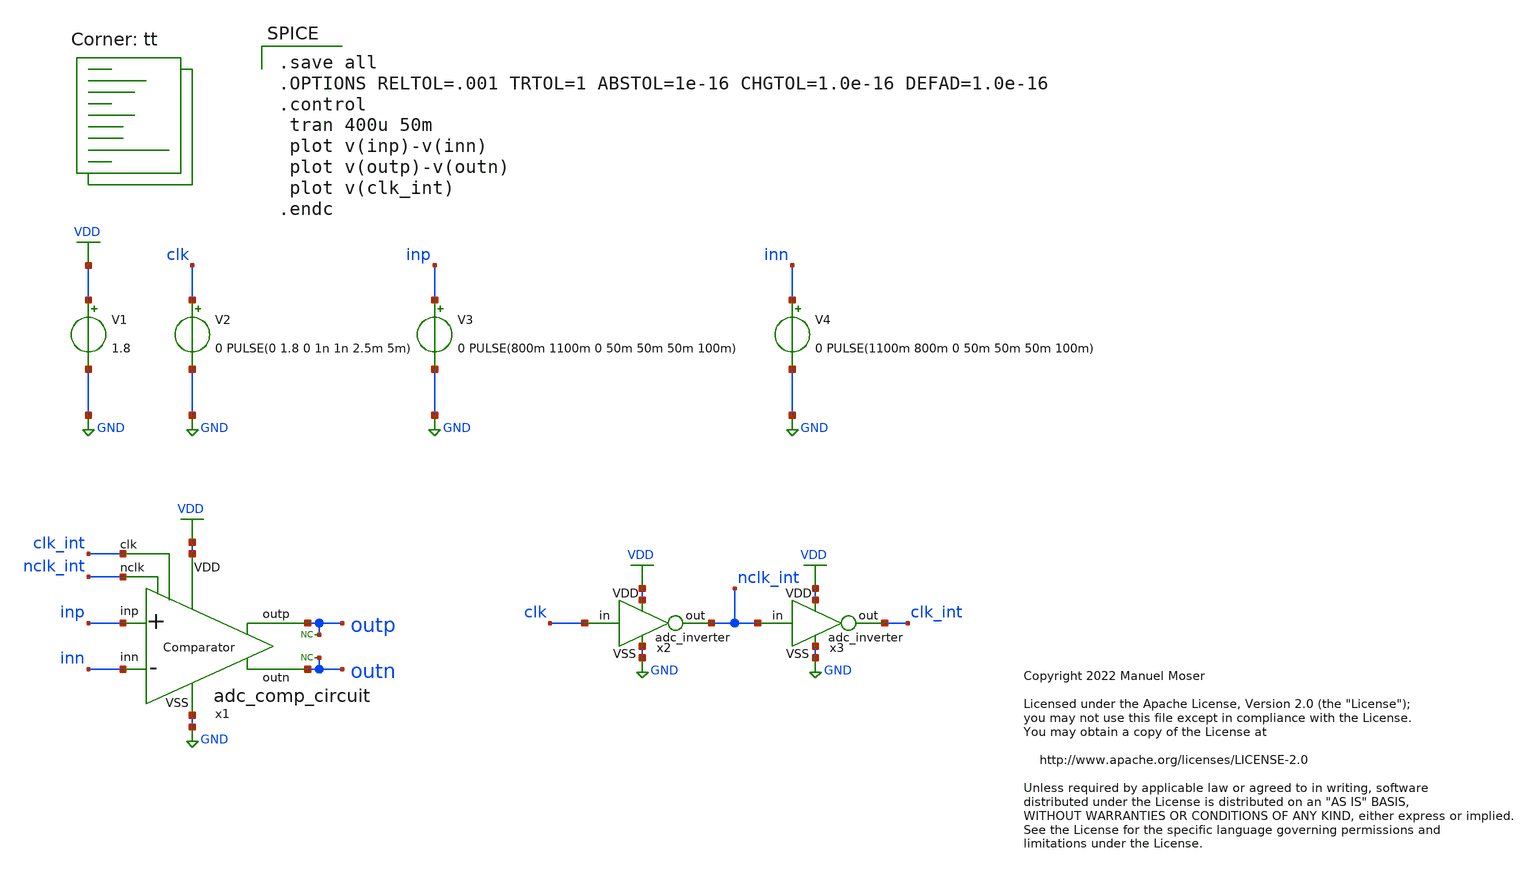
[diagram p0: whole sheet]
** sch_path: xschem/adc_comp_circuit_tb.sch
* Copyright 2022 Manuel Moser
* Licensed under the Apache License, Version 2.0 (the "License");
**.subckt adc_comp_circuit_tb
V1 VDD GND 1.8
V2 clk GND 0 PULSE(0 1.8 0 1n 1n 2.5m 5m)
V3 inp GND 0 PULSE(800m 1100m 0 50m 50m 50m 100m)
V4 inn GND 0 PULSE(1100m 800m 0 50m 50m 50m 100m)
* noconn outp
* noconn outn
x1 VDD clk_int outp inp inn outn nclk_int GND adc_comp_circuit
x2 VDD GND clk nclk_int adc_inverter
x3 VDD GND nclk_int clk_int adc_inverter
**** begin user architecture code
.lib $::SKYWATER_MODELS/sky130.lib.spice tt

.save all
.OPTIONS RELTOL=.001 TRTOL=1 ABSTOL=1e-16 CHGTOL=1.0e-16 DEFAD=1.0e-16
.control
 tran 400u 50m
 plot v(inp)-v(inn)
 plot v(outp)-v(outn)
 plot v(clk_int)
.endc

**** end user architecture code
**.ends

* expanding   symbol:  adc_comp_circuit.sym # of pins=8
** sym_path: xschem/adc_comp_circuit.sym
** sch_path: xschem/adc_comp_circuit.sch
.subckt adc_comp_circuit VDD clk outp inp inn outn nclk VSS
*.iopin VDD
*.iopin VSS
*.ipin inp
*.ipin inn
*.ipin clk
*.ipin nclk
*.opin outp
*.opin outn
XM1 on clk VDD VDD sky130_fd_pr__pfet_01v8 L=0.15 W=2 nf=4 ad='int((nf+1)/2) * W/nf * 0.29' as='int((nf+2)/2) * W/nf * 0.29'
+ pd='2*int((nf+1)/2) * (W/nf + 0.29)' ps='2*int((nf+2)/2) * (W/nf + 0.29)' nrd='0.29 / W' nrs='0.29 / W'
+ sa=0 sb=0 sd=0 mult=1 m=1
XM2 op clk VDD VDD sky130_fd_pr__pfet_01v8 L=0.15 W=2 nf=4 ad='int((nf+1)/2) * W/nf * 0.29' as='int((nf+2)/2) * W/nf * 0.29'
+ pd='2*int((nf+1)/2) * (W/nf + 0.29)' ps='2*int((nf+2)/2) * (W/nf + 0.29)' nrd='0.29 / W' nrs='0.29 / W'
+ sa=0 sb=0 sd=0 mult=1 m=1
XM3 on inp net1 VSS sky130_fd_pr__nfet_01v8 L=0.15 W=8 nf=4 ad='int((nf+1)/2) * W/nf * 0.29' as='int((nf+2)/2) * W/nf * 0.29'
+ pd='2*int((nf+1)/2) * (W/nf + 0.29)' ps='2*int((nf+2)/2) * (W/nf + 0.29)' nrd='0.29 / W' nrs='0.29 / W'
+ sa=0 sb=0 sd=0 mult=1 m=1
XM4 op inn net1 VSS sky130_fd_pr__nfet_01v8 L=0.15 W=8 nf=4 ad='int((nf+1)/2) * W/nf * 0.29' as='int((nf+2)/2) * W/nf * 0.29'
+ pd='2*int((nf+1)/2) * (W/nf + 0.29)' ps='2*int((nf+2)/2) * (W/nf + 0.29)' nrd='0.29 / W' nrs='0.29 / W'
+ sa=0 sb=0 sd=0 mult=1 m=1
XM5 net1 clk VSS VSS sky130_fd_pr__nfet_01v8 L=0.15 W=4 nf=8 ad='int((nf+1)/2) * W/nf * 0.29' as='int((nf+2)/2) * W/nf * 0.29'
+ pd='2*int((nf+1)/2) * (W/nf + 0.29)' ps='2*int((nf+2)/2) * (W/nf + 0.29)' nrd='0.29 / W' nrs='0.29 / W'
+ sa=0 sb=0 sd=0 mult=1 m=1
XM6 net3 bp VDD VDD sky130_fd_pr__pfet_01v8 L=0.15 W=4 nf=2 ad='int((nf+1)/2) * W/nf * 0.29' as='int((nf+2)/2) * W/nf * 0.29'
+ pd='2*int((nf+1)/2) * (W/nf + 0.29)' ps='2*int((nf+2)/2) * (W/nf + 0.29)' nrd='0.29 / W' nrs='0.29 / W'
+ sa=0 sb=0 sd=0 mult=1 m=1
XM7 net2 bn VDD VDD sky130_fd_pr__pfet_01v8 L=0.15 W=4 nf=2 ad='int((nf+1)/2) * W/nf * 0.29' as='int((nf+2)/2) * W/nf * 0.29'
+ pd='2*int((nf+1)/2) * (W/nf + 0.29)' ps='2*int((nf+2)/2) * (W/nf + 0.29)' nrd='0.29 / W' nrs='0.29 / W'
+ sa=0 sb=0 sd=0 mult=1 m=1
XM8 bn op net3 VDD sky130_fd_pr__pfet_01v8 L=0.15 W=4 nf=2 ad='int((nf+1)/2) * W/nf * 0.29' as='int((nf+2)/2) * W/nf * 0.29'
+ pd='2*int((nf+1)/2) * (W/nf + 0.29)' ps='2*int((nf+2)/2) * (W/nf + 0.29)' nrd='0.29 / W' nrs='0.29 / W'
+ sa=0 sb=0 sd=0 mult=1 m=1
XM9 bp on net2 VDD sky130_fd_pr__pfet_01v8 L=0.15 W=4 nf=2 ad='int((nf+1)/2) * W/nf * 0.29' as='int((nf+2)/2) * W/nf * 0.29'
+ pd='2*int((nf+1)/2) * (W/nf + 0.29)' ps='2*int((nf+2)/2) * (W/nf + 0.29)' nrd='0.29 / W' nrs='0.29 / W'
+ sa=0 sb=0 sd=0 mult=1 m=1
XM10 bn bp VSS VSS sky130_fd_pr__nfet_01v8 L=0.15 W=2 nf=1 ad='int((nf+1)/2) * W/nf * 0.29' as='int((nf+2)/2) * W/nf * 0.29'
+ pd='2*int((nf+1)/2) * (W/nf + 0.29)' ps='2*int((nf+2)/2) * (W/nf + 0.29)' nrd='0.29 / W' nrs='0.29 / W'
+ sa=0 sb=0 sd=0 mult=1 m=1
XM11 bn nclk VSS VSS sky130_fd_pr__nfet_01v8 L=0.15 W=2 nf=1 ad='int((nf+1)/2) * W/nf * 0.29' as='int((nf+2)/2) * W/nf * 0.29'
+ pd='2*int((nf+1)/2) * (W/nf + 0.29)' ps='2*int((nf+2)/2) * (W/nf + 0.29)' nrd='0.29 / W' nrs='0.29 / W'
+ sa=0 sb=0 sd=0 mult=1 m=1
XM12 bp nclk VSS VSS sky130_fd_pr__nfet_01v8 L=0.15 W=2 nf=1 ad='int((nf+1)/2) * W/nf * 0.29' as='int((nf+2)/2) * W/nf * 0.29'
+ pd='2*int((nf+1)/2) * (W/nf + 0.29)' ps='2*int((nf+2)/2) * (W/nf + 0.29)' nrd='0.29 / W' nrs='0.29 / W'
+ sa=0 sb=0 sd=0 mult=1 m=1
XM13 bp bn VSS VSS sky130_fd_pr__nfet_01v8 L=0.15 W=2 nf=1 ad='int((nf+1)/2) * W/nf * 0.29' as='int((nf+2)/2) * W/nf * 0.29'
+ pd='2*int((nf+1)/2) * (W/nf + 0.29)' ps='2*int((nf+2)/2) * (W/nf + 0.29)' nrd='0.29 / W' nrs='0.29 / W'
+ sa=0 sb=0 sd=0 mult=1 m=1
x1 VDD VSS bp outp adc_comp_buffer
x2 VDD VSS bn outn adc_comp_buffer
x3 VSS VSS on VSS VSS adc_noise_decoup_cell2
x4 VSS VSS op VSS VSS adc_noise_decoup_cell2
.ends


* expanding   symbol:  adc_inverter.sym # of pins=4
** sym_path: xschem/adc_inverter.sym
** sch_path: xschem/adc_inverter.sch
.subckt adc_inverter VDD VSS in out
*.iopin VDD
*.iopin VSS
*.opin out
*.ipin in
XM1 out in VSS VSS sky130_fd_pr__nfet_01v8 L=0.15 W=0.42 nf=1 ad='int((nf+1)/2) * W/nf * 0.29' as='int((nf+2)/2) * W/nf * 0.29'
+ pd='2*int((nf+1)/2) * (W/nf + 0.29)' ps='2*int((nf+2)/2) * (W/nf + 0.29)' nrd='0.29 / W' nrs='0.29 / W'
+ sa=0 sb=0 sd=0 mult=1 m=1
XM2 out in VDD VDD sky130_fd_pr__pfet_01v8 L=0.15 W=0.84 nf=2 ad='int((nf+1)/2) * W/nf * 0.29' as='int((nf+2)/2) * W/nf * 0.29'
+ pd='2*int((nf+1)/2) * (W/nf + 0.29)' ps='2*int((nf+2)/2) * (W/nf + 0.29)' nrd='0.29 / W' nrs='0.29 / W'
+ sa=0 sb=0 sd=0 mult=1 m=1
.ends


* expanding   symbol:  adc_comp_buffer.sym # of pins=4
** sym_path: xschem/adc_comp_buffer.sym
** sch_path: xschem/adc_comp_buffer.sch
.subckt adc_comp_buffer VDD VSS in out
*.iopin VDD
*.iopin VSS
*.ipin in
*.opin out
XM5 net1 in VSS VSS sky130_fd_pr__nfet_01v8 L=0.15 W=0.5 nf=1 ad='int((nf+1)/2) * W/nf * 0.29' as='int((nf+2)/2) * W/nf * 0.29'
+ pd='2*int((nf+1)/2) * (W/nf + 0.29)' ps='2*int((nf+2)/2) * (W/nf + 0.29)' nrd='0.29 / W' nrs='0.29 / W'
+ sa=0 sb=0 sd=0 mult=1 m=1
XM1 net1 in VDD VDD sky130_fd_pr__pfet_01v8 L=0.15 W=1 nf=1 ad='int((nf+1)/2) * W/nf * 0.29' as='int((nf+2)/2) * W/nf * 0.29'
+ pd='2*int((nf+1)/2) * (W/nf + 0.29)' ps='2*int((nf+2)/2) * (W/nf + 0.29)' nrd='0.29 / W' nrs='0.29 / W'
+ sa=0 sb=0 sd=0 mult=1 m=1
XM2 out net1 VDD VDD sky130_fd_pr__pfet_01v8 L=0.15 W=2 nf=2 ad='int((nf+1)/2) * W/nf * 0.29' as='int((nf+2)/2) * W/nf * 0.29'
+ pd='2*int((nf+1)/2) * (W/nf + 0.29)' ps='2*int((nf+2)/2) * (W/nf + 0.29)' nrd='0.29 / W' nrs='0.29 / W'
+ sa=0 sb=0 sd=0 mult=1 m=1
XM6 out net1 VSS VSS sky130_fd_pr__nfet_01v8 L=0.15 W=1 nf=2 ad='int((nf+1)/2) * W/nf * 0.29' as='int((nf+2)/2) * W/nf * 0.29'
+ pd='2*int((nf+1)/2) * (W/nf + 0.29)' ps='2*int((nf+2)/2) * (W/nf + 0.29)' nrd='0.29 / W' nrs='0.29 / W'
+ sa=0 sb=0 sd=0 mult=1 m=1
.ends


* expanding   symbol:  adc_noise_decoup_cell2.sym # of pins=5
** sym_path: xschem/adc_noise_decoup_cell2.sym
** sch_path: xschem/adc_noise_decoup_cell2.sch
.subckt adc_noise_decoup_cell2 mimcap_top mimcap_bot nmoscap_top nmoscap_bot pwell
*.iopin nmoscap_top
*.iopin mimcap_top
*.iopin mimcap_bot
*.iopin nmoscap_bot
*.iopin pwell
XC1 mimcap_top mimcap_bot sky130_fd_pr__cap_mim_m3_1 W=18.9 L=5.1 MF=1 m=1
XC2 nmoscap_top nmoscap_bot pwell sky130_fd_pr__cap_var_lvt W=18.4 L=3.9 VM=1 m=1
.ends

.GLOBAL GND
.GLOBAL VDD
.end
